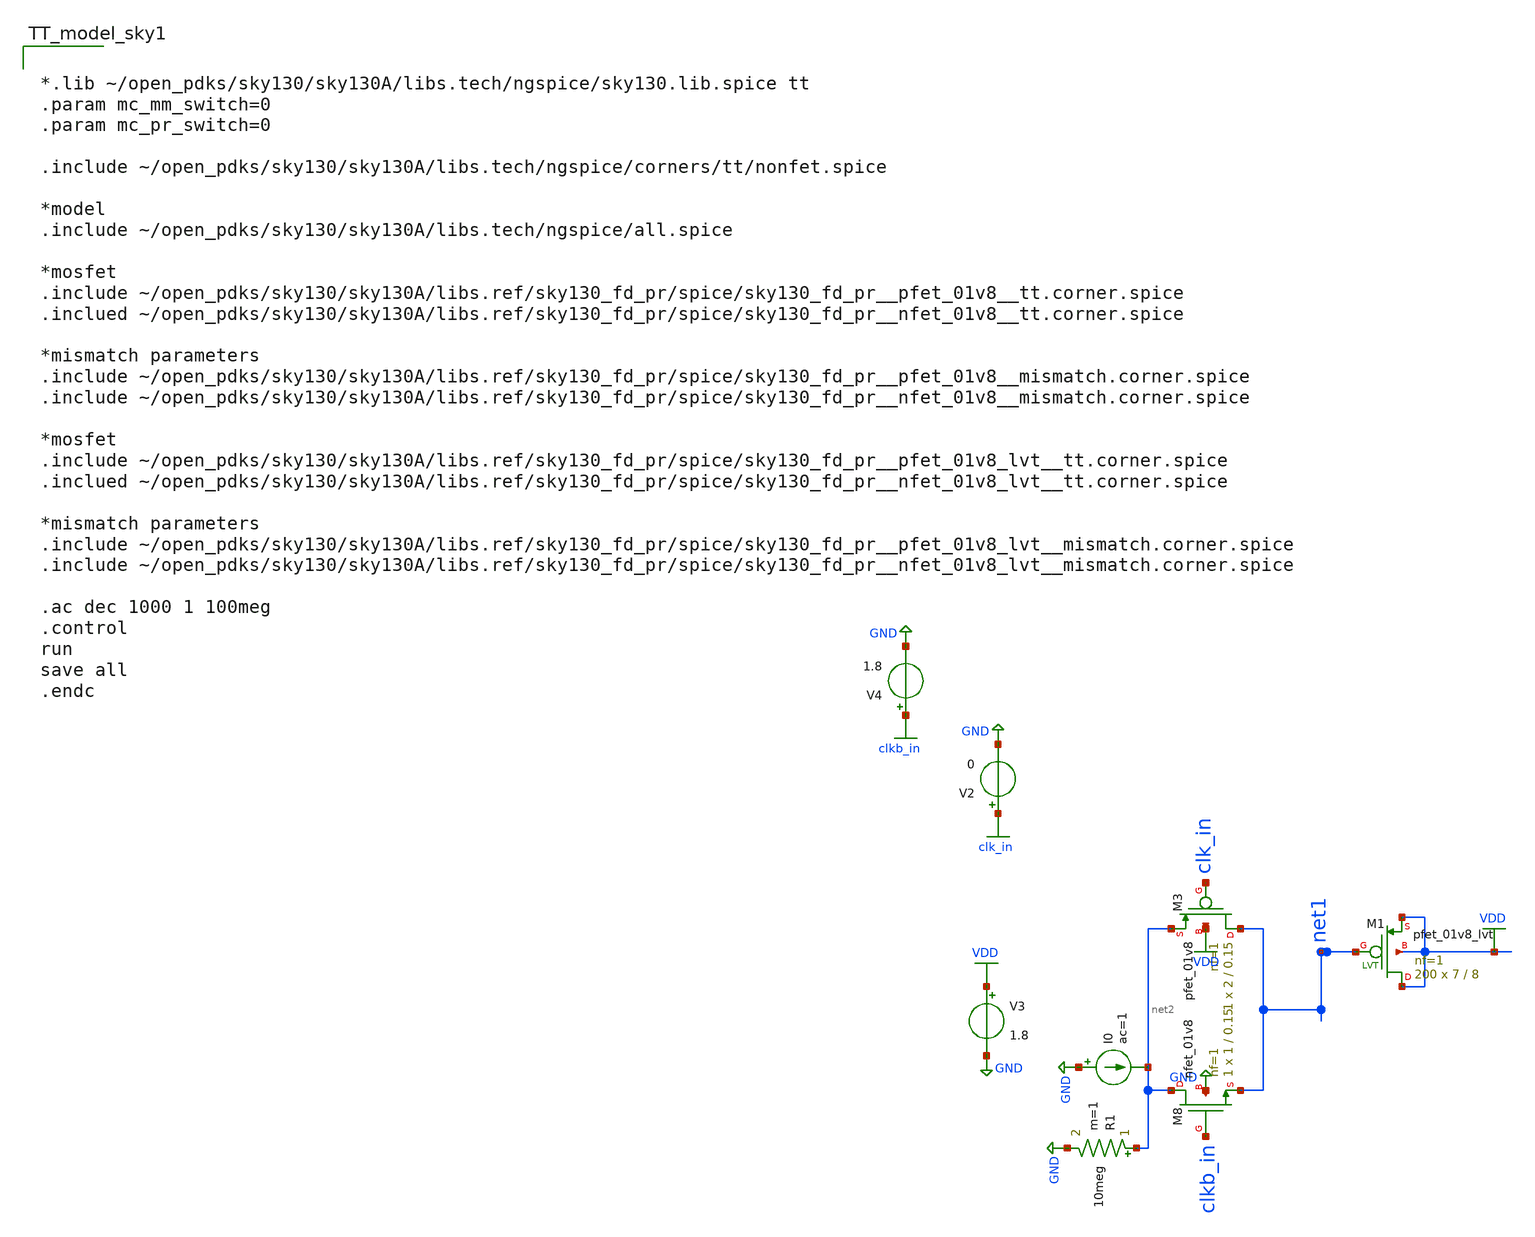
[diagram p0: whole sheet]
** sch_path: Schematics/Switched capacitor/tran.sch
**.subckt tran
V3 VDD GND 1.8
XM3 net1 clk_in net2 VDD sky130_fd_pr__pfet_01v8 L=0.15 W=2 nf=1 ad='int((nf+1)/2) * W/nf * 0.29' as='int((nf+2)/2) * W/nf * 0.29'
+ pd='2*int((nf+1)/2) * (W/nf + 0.29)' ps='2*int((nf+2)/2) * (W/nf + 0.29)' nrd='0.29 / W' nrs='0.29 / W'
+ sa=0 sb=0 sd=0 mult=1 m=1
XM8 net2 clkb_in net1 GND sky130_fd_pr__nfet_01v8 L=0.15 W=1 nf=1 ad='int((nf+1)/2) * W/nf * 0.29' as='int((nf+2)/2) * W/nf * 0.29'
+ pd='2*int((nf+1)/2) * (W/nf + 0.29)' ps='2*int((nf+2)/2) * (W/nf + 0.29)' nrd='0.29 / W' nrs='0.29 / W'
+ sa=0 sb=0 sd=0 mult=1 m=1
V2 clk_in GND 0
V4 clkb_in GND 1.8
XM1 VDD net1 VDD VDD sky130_fd_pr__pfet_01v8_lvt L=8 W=7 nf=1 ad='int((nf+1)/2) * W/nf * 0.29' as='int((nf+2)/2) * W/nf * 0.29'
+ pd='2*int((nf+1)/2) * (W/nf + 0.29)' ps='2*int((nf+2)/2) * (W/nf + 0.29)' nrd='0.29 / W' nrs='0.29 / W'
+ sa=0 sb=0 sd=0 mult=200 m=200
R1 net2 GND 10meg m=1
I0 GND net2 ac=1
**** begin user architecture code

*.lib ~/open_pdks/sky130/sky130A/libs.tech/ngspice/sky130.lib.spice tt
.param mc_mm_switch=0
.param mc_pr_switch=0

.include ~/open_pdks/sky130/sky130A/libs.tech/ngspice/corners/tt/nonfet.spice

*model
.include ~/open_pdks/sky130/sky130A/libs.tech/ngspice/all.spice

*mosfet
.include ~/open_pdks/sky130/sky130A/libs.ref/sky130_fd_pr/spice/sky130_fd_pr__pfet_01v8__tt.corner.spice
.inclued ~/open_pdks/sky130/sky130A/libs.ref/sky130_fd_pr/spice/sky130_fd_pr__nfet_01v8__tt.corner.spice

*mismatch parameters
.include ~/open_pdks/sky130/sky130A/libs.ref/sky130_fd_pr/spice/sky130_fd_pr__pfet_01v8__mismatch.corner.spice
.include ~/open_pdks/sky130/sky130A/libs.ref/sky130_fd_pr/spice/sky130_fd_pr__nfet_01v8__mismatch.corner.spice

*mosfet
.include ~/open_pdks/sky130/sky130A/libs.ref/sky130_fd_pr/spice/sky130_fd_pr__pfet_01v8_lvt__tt.corner.spice
.inclued ~/open_pdks/sky130/sky130A/libs.ref/sky130_fd_pr/spice/sky130_fd_pr__nfet_01v8_lvt__tt.corner.spice

*mismatch parameters
.include ~/open_pdks/sky130/sky130A/libs.ref/sky130_fd_pr/spice/sky130_fd_pr__pfet_01v8_lvt__mismatch.corner.spice
.include ~/open_pdks/sky130/sky130A/libs.ref/sky130_fd_pr/spice/sky130_fd_pr__nfet_01v8_lvt__mismatch.corner.spice

.ac dec 1000 1 100meg
.control
run
save all
.endc
**** end user architecture code
**.ends
.GLOBAL GND
.GLOBAL VDD
.GLOBAL clk_in
.GLOBAL clkb_in
.end
